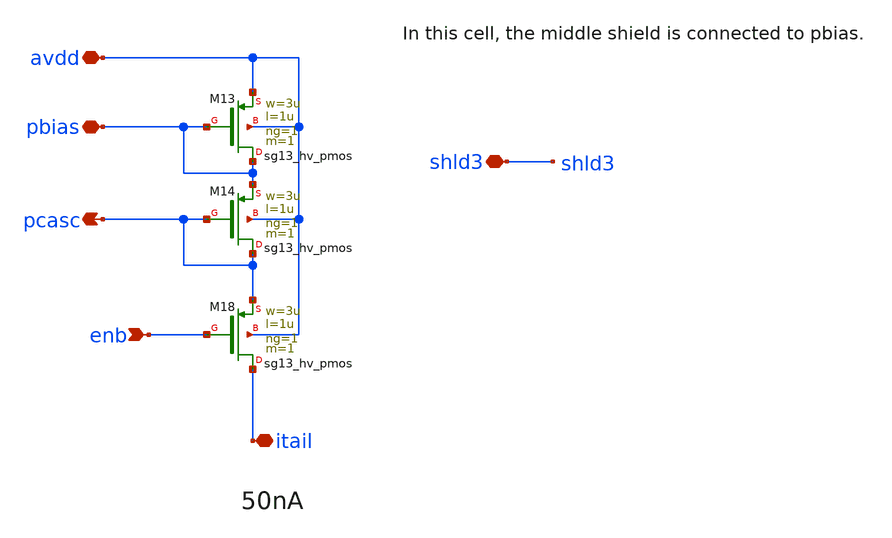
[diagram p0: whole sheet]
** sch_path: xschem/bias_pset.sch
**.subckt bias_pset pbias itail enb pcasc avdd shld3
*.iopin pbias
*.iopin itail
*.ipin enb
*.opin pcasc
*.iopin avdd
*.iopin shld3
XM13 pbias pbias avdd avdd sg13_hv_pmos w=3u l=1u ng=1 m=1 mm_ok=1
XM18 itail enb pcasc avdd sg13_hv_pmos w=3u l=1u ng=1 m=1 mm_ok=1
XM14 pcasc pcasc pbias avdd sg13_hv_pmos w=3u l=1u ng=1 m=1 mm_ok=1
**.ends
.end
